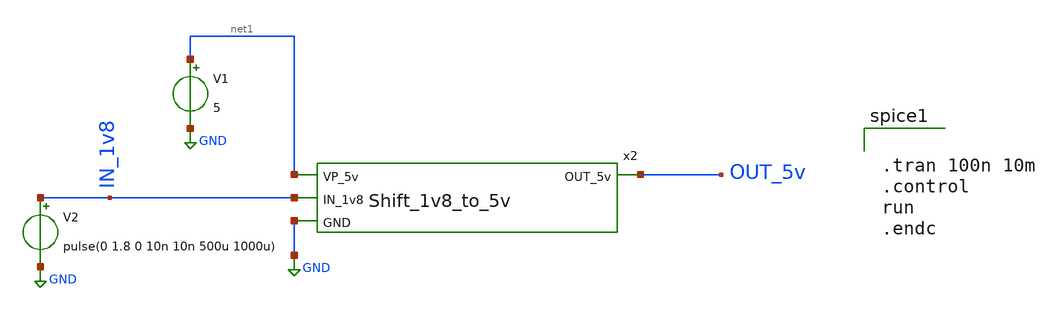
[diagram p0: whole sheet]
** sch_path: ADC/4bit_C2C/MagicAndSpice/EE431_FinalProj/shift_up_tb.sch
**.subckt shift_up_tb
V1 net1 GND 5
V2 IN_1v8 GND pulse(0 1.8 0 10n 10n 500u 1000u)
x2 net1 OUT_5v IN_1v8 GND Shift_1v8_to_5v
**** begin user architecture code
 .lib $::SKYWATER_MODELS/sky130.lib.spice tt


.tran 100n 10m
.control
run
.endc

**** end user architecture code
**.ends
.GLOBAL GND
.end
